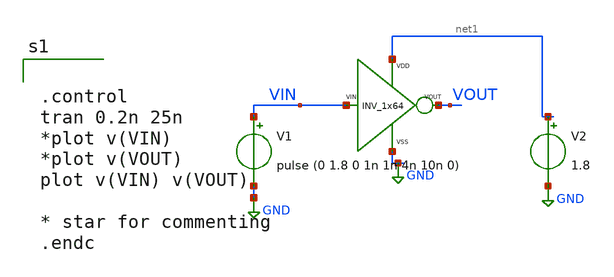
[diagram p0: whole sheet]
** sch_path: xschem/xschem_BGR_Top/Sigma_Delta/INV_1x64/INV_1x64_TB.sch
**.subckt INV_1x64_TB
V1 VIN GND pulse (0 1.8 0 1n 1n 4n 10n 0)
V2 net1 GND 1.8
X1 GND net1 VIN VOUT INV_1x64
**** begin user architecture code


.control
tran 0.2n 25n
*plot v(VIN)
*plot v(VOUT)
plot v(VIN) v(VOUT)

* star for commenting
.endc


** opencircuitdesign pdks install
.lib $::SKYWATER_MODELS/sky130.lib.spice tt


**** end user architecture code
**.ends

* expanding   symbol:  Sigma_Delta/INV_1x64/INV_1x64.sym # of pins=4
** sym_path: xschem/xschem_BGR_Top/Sigma_Delta/INV_1x64/INV_1x64.sym
** sch_path: xschem/xschem_BGR_Top/Sigma_Delta/INV_1x64/INV_1x64.sch
.subckt INV_1x64 VSS VDD VIN VOUT
*.ipin VIN
*.iopin VDD
*.iopin VSS
*.opin VOUT
XM1 VOUT VIN net1 VSS sky130_fd_pr__nfet_01v8 L=0.15 W=0.425 nf=1 ad='int((nf+1)/2) * W/nf * 0.29' as='int((nf+2)/2) * W/nf * 0.29'
+ pd='2*int((nf+1)/2) * (W/nf + 0.29)' ps='2*int((nf+2)/2) * (W/nf + 0.29)' nrd='0.29 / W' nrs='0.29 / W'
+ sa=0 sb=0 sd=0 mult=1 m=1
XM2 VOUT VIN net2 VDD sky130_fd_pr__pfet_01v8 L=0.15 W=0.425 nf=1 ad='int((nf+1)/2) * W/nf * 0.29' as='int((nf+2)/2) * W/nf * 0.29'
+ pd='2*int((nf+1)/2) * (W/nf + 0.29)' ps='2*int((nf+2)/2) * (W/nf + 0.29)' nrd='0.29 / W' nrs='0.29 / W'
+ sa=0 sb=0 sd=0 mult=1 m=1
XM3 net2 VIN net3 VDD sky130_fd_pr__pfet_01v8 L=0.15 W=0.425 nf=1 ad='int((nf+1)/2) * W/nf * 0.29' as='int((nf+2)/2) * W/nf * 0.29'
+ pd='2*int((nf+1)/2) * (W/nf + 0.29)' ps='2*int((nf+2)/2) * (W/nf + 0.29)' nrd='0.29 / W' nrs='0.29 / W'
+ sa=0 sb=0 sd=0 mult=1 m=1
XM4 net3 VIN net4 VDD sky130_fd_pr__pfet_01v8 L=0.15 W=0.425 nf=1 ad='int((nf+1)/2) * W/nf * 0.29' as='int((nf+2)/2) * W/nf * 0.29'
+ pd='2*int((nf+1)/2) * (W/nf + 0.29)' ps='2*int((nf+2)/2) * (W/nf + 0.29)' nrd='0.29 / W' nrs='0.29 / W'
+ sa=0 sb=0 sd=0 mult=1 m=1
XM5 net4 VIN net8 VDD sky130_fd_pr__pfet_01v8 L=0.15 W=0.425 nf=1 ad='int((nf+1)/2) * W/nf * 0.29' as='int((nf+2)/2) * W/nf * 0.29'
+ pd='2*int((nf+1)/2) * (W/nf + 0.29)' ps='2*int((nf+2)/2) * (W/nf + 0.29)' nrd='0.29 / W' nrs='0.29 / W'
+ sa=0 sb=0 sd=0 mult=1 m=1
XM6 net1 VIN net5 VSS sky130_fd_pr__nfet_01v8 L=0.15 W=0.425 nf=1 ad='int((nf+1)/2) * W/nf * 0.29' as='int((nf+2)/2) * W/nf * 0.29'
+ pd='2*int((nf+1)/2) * (W/nf + 0.29)' ps='2*int((nf+2)/2) * (W/nf + 0.29)' nrd='0.29 / W' nrs='0.29 / W'
+ sa=0 sb=0 sd=0 mult=1 m=1
XM7 net5 VIN net6 VSS sky130_fd_pr__nfet_01v8 L=0.15 W=0.425 nf=1 ad='int((nf+1)/2) * W/nf * 0.29' as='int((nf+2)/2) * W/nf * 0.29'
+ pd='2*int((nf+1)/2) * (W/nf + 0.29)' ps='2*int((nf+2)/2) * (W/nf + 0.29)' nrd='0.29 / W' nrs='0.29 / W'
+ sa=0 sb=0 sd=0 mult=1 m=1
XM8 net6 VIN net7 VSS sky130_fd_pr__nfet_01v8 L=0.15 W=0.425 nf=1 ad='int((nf+1)/2) * W/nf * 0.29' as='int((nf+2)/2) * W/nf * 0.29'
+ pd='2*int((nf+1)/2) * (W/nf + 0.29)' ps='2*int((nf+2)/2) * (W/nf + 0.29)' nrd='0.29 / W' nrs='0.29 / W'
+ sa=0 sb=0 sd=0 mult=1 m=1
XM9 net7 VIN VSS VSS sky130_fd_pr__nfet_01v8 L=0.15 W=0.425 nf=1 ad='int((nf+1)/2) * W/nf * 0.29' as='int((nf+2)/2) * W/nf * 0.29'
+ pd='2*int((nf+1)/2) * (W/nf + 0.29)' ps='2*int((nf+2)/2) * (W/nf + 0.29)' nrd='0.29 / W' nrs='0.29 / W'
+ sa=0 sb=0 sd=0 mult=1 m=1
XM10 net8 VIN VDD VDD sky130_fd_pr__pfet_01v8 L=0.15 W=0.425 nf=1 ad='int((nf+1)/2) * W/nf * 0.29' as='int((nf+2)/2) * W/nf * 0.29'
+ pd='2*int((nf+1)/2) * (W/nf + 0.29)' ps='2*int((nf+2)/2) * (W/nf + 0.29)' nrd='0.29 / W' nrs='0.29 / W'
+ sa=0 sb=0 sd=0 mult=1 m=1
.ends

.GLOBAL GND
.end
